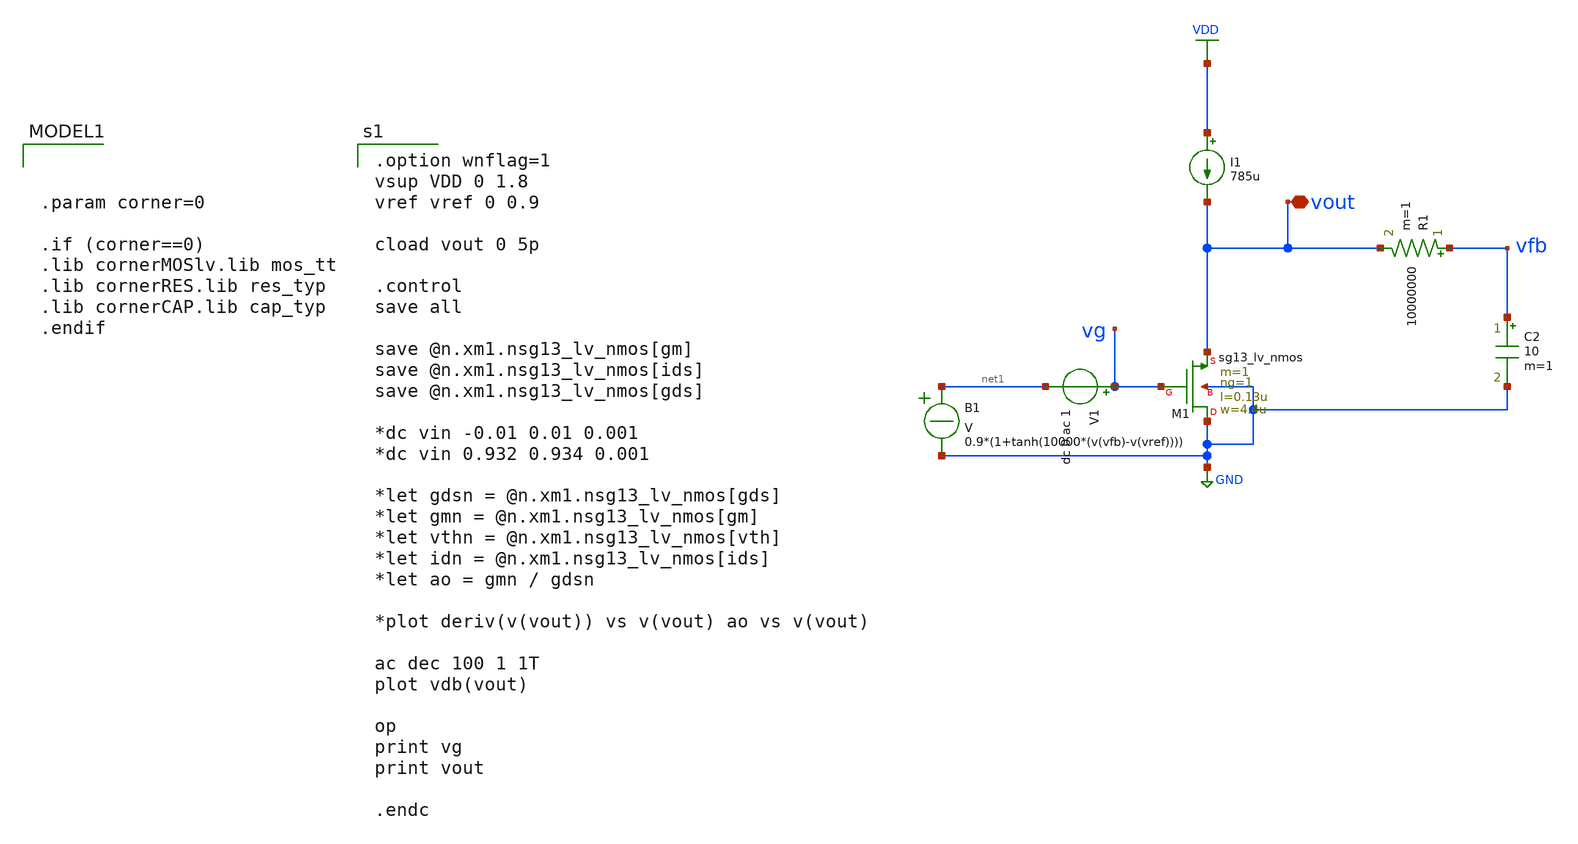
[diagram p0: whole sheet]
** sch_path: xschem/Tareas/Tarea_1/cs_amp_full_FIXED_IPD413HW1.sch
**.subckt cs_amp_full_FIXED_IPD413HW1 vout
*.iopin vout
I1 VDD vout 785u
XM1 GND vg vout GND sg13_lv_nmos w=4.4u l=0.13u ng=1 m=1 mm_ok=1
B1 net1 GND V = 0.9*(1+tanh(10000*(v(vfb)-v(vref))))
V1 vg net1 dc 0 ac 1
R1 vfb vout 10000000 m=1
C2 vfb GND 10 m=1
**** begin user architecture code

.option wnflag=1
vsup VDD 0 1.8
vref vref 0 0.9

cload vout 0 5p

.control
save all

save @n.xm1.nsg13_lv_nmos[gm]
save @n.xm1.nsg13_lv_nmos[ids]
save @n.xm1.nsg13_lv_nmos[gds]

*dc vin -0.01 0.01 0.001
*dc vin 0.932 0.934 0.001

*let gdsn = @n.xm1.nsg13_lv_nmos[gds]
*let gmn = @n.xm1.nsg13_lv_nmos[gm]
*let vthn = @n.xm1.nsg13_lv_nmos[vth]
*let idn = @n.xm1.nsg13_lv_nmos[ids]
*let ao = gmn / gdsn

*plot deriv(v(vout)) vs v(vout) ao vs v(vout)

ac dec 100 1 1T
plot vdb(vout)

op
print vg
print vout

.endc



.param corner=0

.if (corner==0)
.lib cornerMOSlv.lib mos_tt
.lib cornerRES.lib res_typ
.lib cornerCAP.lib cap_typ
.endif

**** end user architecture code
**.ends
.GLOBAL GND
.GLOBAL VDD
.end
